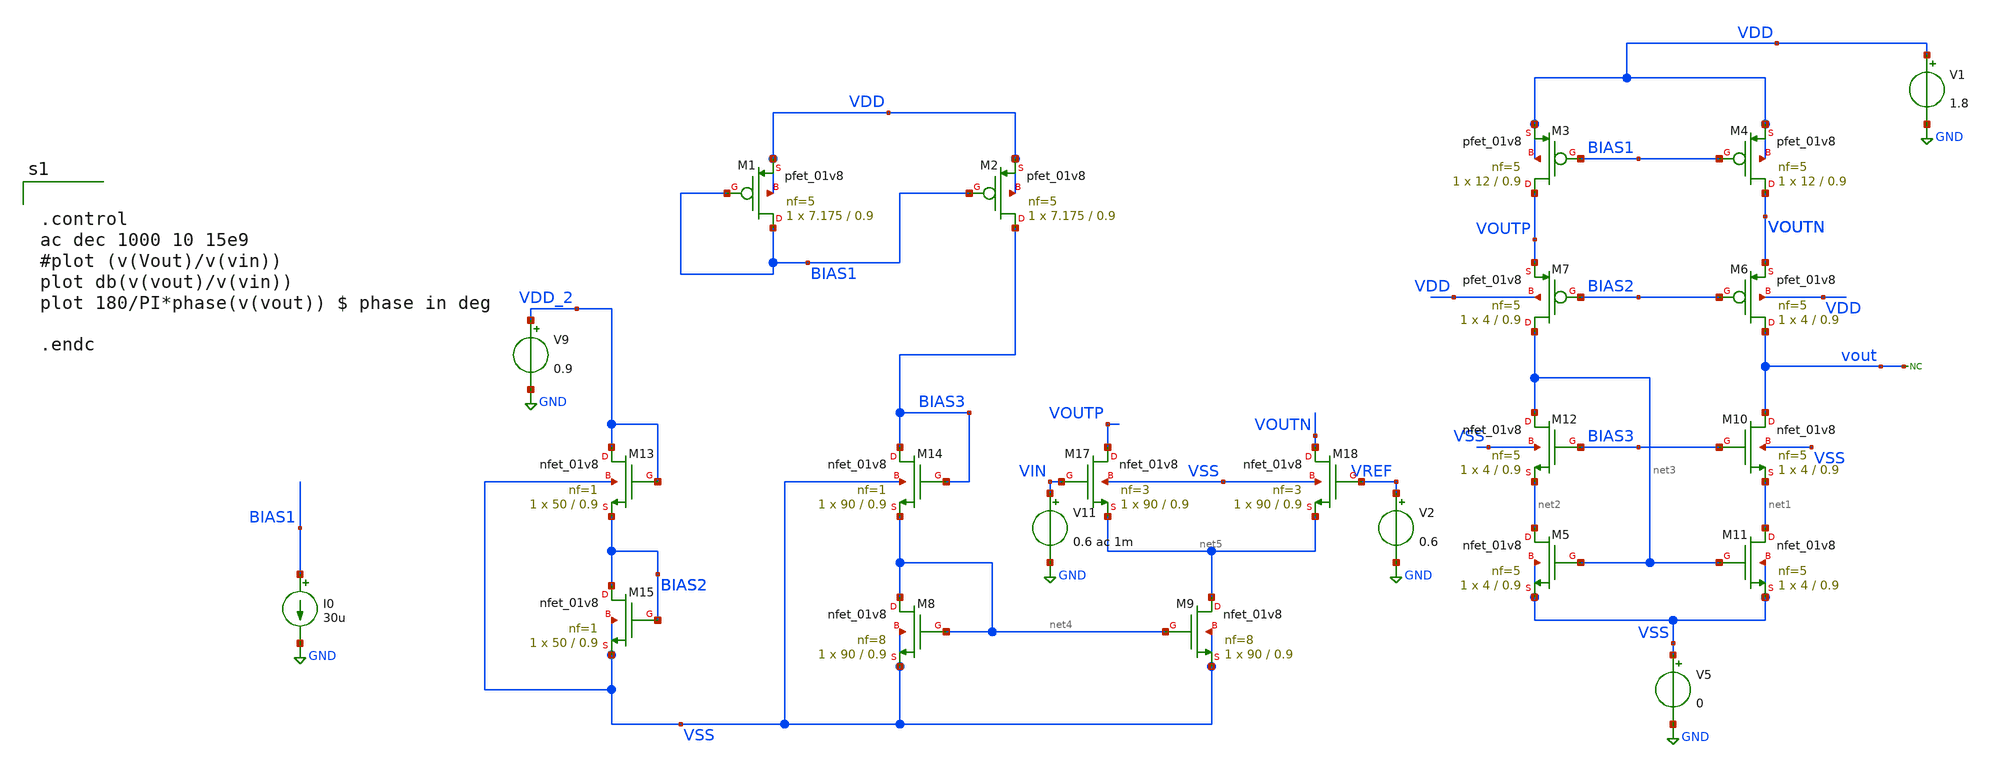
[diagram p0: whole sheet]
** sch_path: xschem/DC_DC_Converter_xschem/OTHERS/DC_DC_Converter_4/Folded_OPAMP.sch
**.subckt Folded_OPAMP
V1 VDD GND 1.8
V5 VSS GND 0
I0 BIAS1 GND 30u
V9 VDD_2 GND 0.9
V11 VIN GND 0.6 ac 1m
XM3 VOUTP BIAS1 VDD VDD sky130_fd_pr__pfet_01v8 L=0.9 W=12 nf=5 ad='int((nf+1)/2) * W/nf * 0.29' as='int((nf+2)/2) * W/nf * 0.29'
+ pd='2*int((nf+1)/2) * (W/nf + 0.29)' ps='2*int((nf+2)/2) * (W/nf + 0.29)' nrd='0.29 / W' nrs='0.29 / W'
+ sa=0 sb=0 sd=0 mult=1 m=1
XM4 VOUTN BIAS1 VDD VDD sky130_fd_pr__pfet_01v8 L=0.9 W=12 nf=5 ad='int((nf+1)/2) * W/nf * 0.29' as='int((nf+2)/2) * W/nf * 0.29'
+ pd='2*int((nf+1)/2) * (W/nf + 0.29)' ps='2*int((nf+2)/2) * (W/nf + 0.29)' nrd='0.29 / W' nrs='0.29 / W'
+ sa=0 sb=0 sd=0 mult=1 m=1
XM6 vout BIAS2 VOUTN VDD sky130_fd_pr__pfet_01v8 L=0.9 W=4 nf=5 ad='int((nf+1)/2) * W/nf * 0.29' as='int((nf+2)/2) * W/nf * 0.29'
+ pd='2*int((nf+1)/2) * (W/nf + 0.29)' ps='2*int((nf+2)/2) * (W/nf + 0.29)' nrd='0.29 / W' nrs='0.29 / W'
+ sa=0 sb=0 sd=0 mult=1 m=1
XM7 net3 BIAS2 VOUTP VDD sky130_fd_pr__pfet_01v8 L=0.9 W=4 nf=5 ad='int((nf+1)/2) * W/nf * 0.29' as='int((nf+2)/2) * W/nf * 0.29'
+ pd='2*int((nf+1)/2) * (W/nf + 0.29)' ps='2*int((nf+2)/2) * (W/nf + 0.29)' nrd='0.29 / W' nrs='0.29 / W'
+ sa=0 sb=0 sd=0 mult=1 m=1
XM13 VDD_2 VDD_2 BIAS2 VSS sky130_fd_pr__nfet_01v8 L=0.9 W=50 nf=1 ad='int((nf+1)/2) * W/nf * 0.29' as='int((nf+2)/2) * W/nf * 0.29'
+ pd='2*int((nf+1)/2) * (W/nf + 0.29)' ps='2*int((nf+2)/2) * (W/nf + 0.29)' nrd='0.29 / W' nrs='0.29 / W'
+ sa=0 sb=0 sd=0 mult=1 m=1
XM14 BIAS3 BIAS3 net4 VSS sky130_fd_pr__nfet_01v8 L=0.9 W=90 nf=1 ad='int((nf+1)/2) * W/nf * 0.29' as='int((nf+2)/2) * W/nf * 0.29'
+ pd='2*int((nf+1)/2) * (W/nf + 0.29)' ps='2*int((nf+2)/2) * (W/nf + 0.29)' nrd='0.29 / W' nrs='0.29 / W'
+ sa=0 sb=0 sd=0 mult=1 m=1
XM15 BIAS2 BIAS2 VSS VSS sky130_fd_pr__nfet_01v8 L=0.9 W=50 nf=1 ad='int((nf+1)/2) * W/nf * 0.29' as='int((nf+2)/2) * W/nf * 0.29'
+ pd='2*int((nf+1)/2) * (W/nf + 0.29)' ps='2*int((nf+2)/2) * (W/nf + 0.29)' nrd='0.29 / W' nrs='0.29 / W'
+ sa=0 sb=0 sd=0 mult=1 m=1
XM17 VOUTP VIN net5 VSS sky130_fd_pr__nfet_01v8 L=0.9 W=90 nf=3 ad='int((nf+1)/2) * W/nf * 0.29' as='int((nf+2)/2) * W/nf * 0.29'
+ pd='2*int((nf+1)/2) * (W/nf + 0.29)' ps='2*int((nf+2)/2) * (W/nf + 0.29)' nrd='0.29 / W' nrs='0.29 / W'
+ sa=0 sb=0 sd=0 mult=1 m=1
XM18 VOUTN VREF net5 VSS sky130_fd_pr__nfet_01v8 L=0.9 W=90 nf=3 ad='int((nf+1)/2) * W/nf * 0.29' as='int((nf+2)/2) * W/nf * 0.29'
+ pd='2*int((nf+1)/2) * (W/nf + 0.29)' ps='2*int((nf+2)/2) * (W/nf + 0.29)' nrd='0.29 / W' nrs='0.29 / W'
+ sa=0 sb=0 sd=0 mult=1 m=1
XM10 vout BIAS3 net1 VSS sky130_fd_pr__nfet_01v8 L=0.9 W=4 nf=5 ad='int((nf+1)/2) * W/nf * 0.29' as='int((nf+2)/2) * W/nf * 0.29'
+ pd='2*int((nf+1)/2) * (W/nf + 0.29)' ps='2*int((nf+2)/2) * (W/nf + 0.29)' nrd='0.29 / W' nrs='0.29 / W'
+ sa=0 sb=0 sd=0 mult=1 m=1
XM12 net3 BIAS3 net2 VSS sky130_fd_pr__nfet_01v8 L=0.9 W=4 nf=5 ad='int((nf+1)/2) * W/nf * 0.29' as='int((nf+2)/2) * W/nf * 0.29'
+ pd='2*int((nf+1)/2) * (W/nf + 0.29)' ps='2*int((nf+2)/2) * (W/nf + 0.29)' nrd='0.29 / W' nrs='0.29 / W'
+ sa=0 sb=0 sd=0 mult=1 m=1
XM8 net4 net4 VSS VSS sky130_fd_pr__nfet_01v8 L=0.9 W=90 nf=8 ad='int((nf+1)/2) * W/nf * 0.29' as='int((nf+2)/2) * W/nf * 0.29'
+ pd='2*int((nf+1)/2) * (W/nf + 0.29)' ps='2*int((nf+2)/2) * (W/nf + 0.29)' nrd='0.29 / W' nrs='0.29 / W'
+ sa=0 sb=0 sd=0 mult=1 m=1
XM9 net5 net4 VSS VSS sky130_fd_pr__nfet_01v8 L=0.9 W=90 nf=8 ad='int((nf+1)/2) * W/nf * 0.29' as='int((nf+2)/2) * W/nf * 0.29'
+ pd='2*int((nf+1)/2) * (W/nf + 0.29)' ps='2*int((nf+2)/2) * (W/nf + 0.29)' nrd='0.29 / W' nrs='0.29 / W'
+ sa=0 sb=0 sd=0 mult=1 m=1
XM5 net2 net3 VSS VSS sky130_fd_pr__nfet_01v8 L=0.9 W=4 nf=5 ad='int((nf+1)/2) * W/nf * 0.29' as='int((nf+2)/2) * W/nf * 0.29'
+ pd='2*int((nf+1)/2) * (W/nf + 0.29)' ps='2*int((nf+2)/2) * (W/nf + 0.29)' nrd='0.29 / W' nrs='0.29 / W'
+ sa=0 sb=0 sd=0 mult=1 m=1
XM11 net1 net3 VSS VSS sky130_fd_pr__nfet_01v8 L=0.9 W=4 nf=5 ad='int((nf+1)/2) * W/nf * 0.29' as='int((nf+2)/2) * W/nf * 0.29'
+ pd='2*int((nf+1)/2) * (W/nf + 0.29)' ps='2*int((nf+2)/2) * (W/nf + 0.29)' nrd='0.29 / W' nrs='0.29 / W'
+ sa=0 sb=0 sd=0 mult=1 m=1
XM1 BIAS1 BIAS1 VDD VDD sky130_fd_pr__pfet_01v8 L=0.9 W=7.175 nf=5 ad='int((nf+1)/2) * W/nf * 0.29' as='int((nf+2)/2) * W/nf * 0.29'
+ pd='2*int((nf+1)/2) * (W/nf + 0.29)' ps='2*int((nf+2)/2) * (W/nf + 0.29)' nrd='0.29 / W' nrs='0.29 / W'
+ sa=0 sb=0 sd=0 mult=1 m=1
XM2 BIAS3 BIAS1 VDD VDD sky130_fd_pr__pfet_01v8 L=0.9 W=7.175 nf=5 ad='int((nf+1)/2) * W/nf * 0.29' as='int((nf+2)/2) * W/nf * 0.29'
+ pd='2*int((nf+1)/2) * (W/nf + 0.29)' ps='2*int((nf+2)/2) * (W/nf + 0.29)' nrd='0.29 / W' nrs='0.29 / W'
+ sa=0 sb=0 sd=0 mult=1 m=1
V2 VREF GND 0.6
* noconn vout
**** begin user architecture code

** opencircuitdesign pdks install
.lib $::SKYWATER_MODELS/sky130.lib.spice tt




.control
ac dec 1000 10 15e9
#plot (v(Vout)/v(vin))
plot db(v(vout)/v(vin))
plot 180/PI*phase(v(vout)) $ phase in deg

.endc


**** end user architecture code
**.ends
.GLOBAL GND
.end
